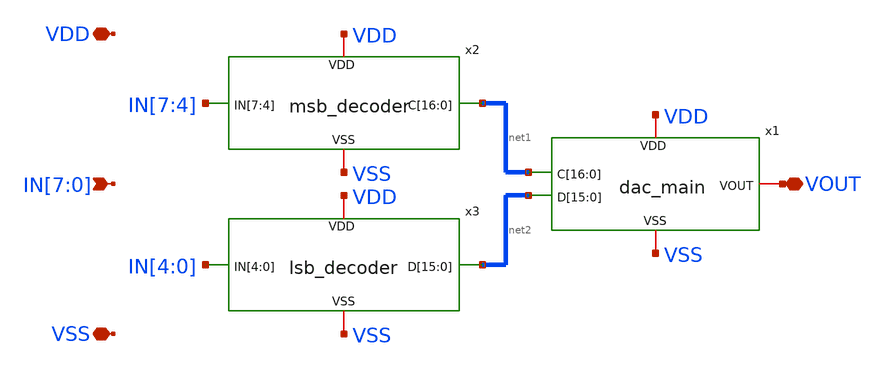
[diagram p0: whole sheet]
** sch_path: xschem/dac.sch
**.subckt dac VDD VSS IN[7],IN[6],IN[5],IN[4],IN[3],IN[2],IN[1],IN[0] VOUT
*.iopin VDD
*.iopin VSS
*.ipin IN[7],IN[6],IN[5],IN[4],IN[3],IN[2],IN[1],IN[0]
*.iopin VOUT
x1 VDD net1[16] net1[15] net1[14] net1[13] net1[12] net1[11] net1[10] net1[9] net1[8] net1[7]
+ net1[6] net1[5] net1[4] net1[3] net1[2] net1[1] net1[0] VOUT net2[15] net2[14] net2[13] net2[12] net2[11]
+ net2[10] net2[9] net2[8] net2[7] net2[6] net2[5] net2[4] net2[3] net2[2] net2[1] net2[0] VSS dac_main
x2 VDD IN[7] IN[6] IN[5] IN[4] net1[16] net1[15] net1[14] net1[13] net1[12] net1[11] net1[10]
+ net1[9] net1[8] net1[7] net1[6] net1[5] net1[4] net1[3] net1[2] net1[1] net1[0] VSS msb_decoder
x3 VDD IN[4] IN[3] IN[2] IN[1] IN[0] net2[15] net2[14] net2[13] net2[12] net2[11] net2[10] net2[9]
+ net2[8] net2[7] net2[6] net2[5] net2[4] net2[3] net2[2] net2[1] net2[0] VSS lsb_decoder
**.ends
.end
